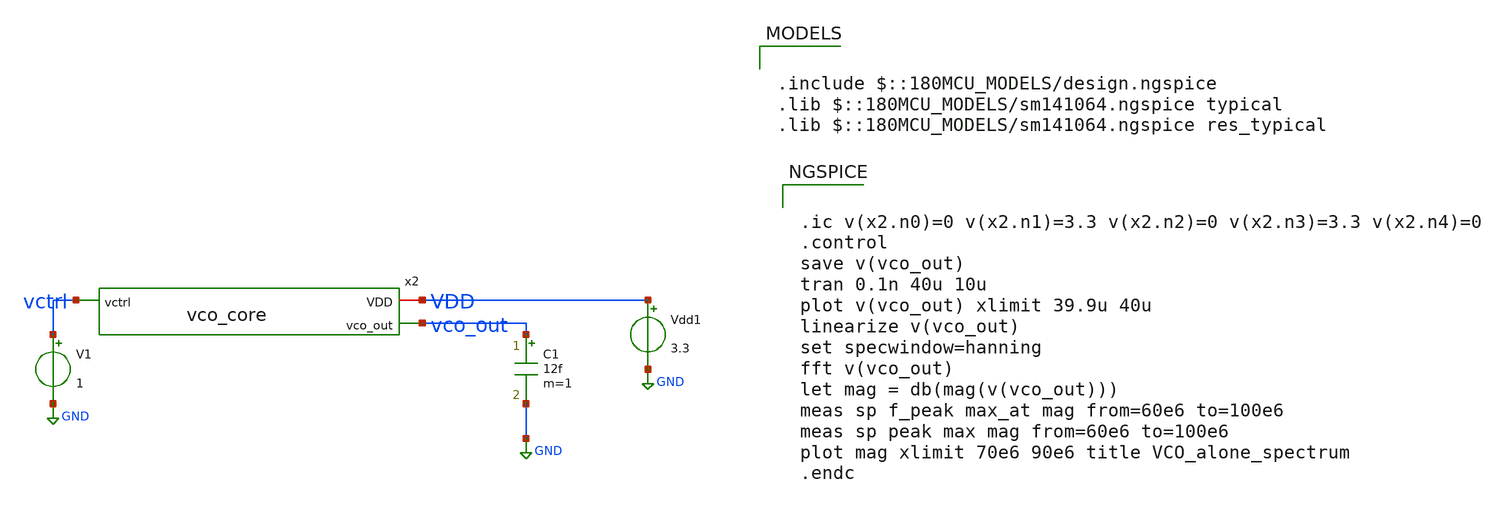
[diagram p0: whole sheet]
** sch_path: xschem/pll_dac/tb_vco_fft.sch
**.subckt tb_vco_fft
x2 VDD vctrl vco_out vco_core
C1 vco_out GND 12f m=1
V1 vctrl GND 1
Vdd1 VDD GND 3.3
**** begin user architecture code

.include $::180MCU_MODELS/design.ngspice
.lib $::180MCU_MODELS/sm141064.ngspice typical
.lib $::180MCU_MODELS/sm141064.ngspice res_typical



.ic v(x2.n0)=0 v(x2.n1)=3.3 v(x2.n2)=0 v(x2.n3)=3.3 v(x2.n4)=0
.control
save v(vco_out)
tran 0.1n 40u 10u
plot v(vco_out) xlimit 39.9u 40u
linearize v(vco_out)
set specwindow=hanning
fft v(vco_out)
let mag = db(mag(v(vco_out)))
meas sp f_peak max_at mag from=60e6 to=100e6
meas sp peak max mag from=60e6 to=100e6
plot mag xlimit 70e6 90e6 title VCO_alone_spectrum
.endc


**** end user architecture code
**.ends

* expanding   symbol:  GF180-PLL/analog/vco/vco_core.sym # of pins=3
** sym_path: analog/vco/vco_core.sym
** sch_path: analog/vco/vco_core.sch
.subckt vco_core VDD vctrl vco_out
*.iopin VDD
*.ipin vctrl
*.opin vco_out
XM1 Vbiasn vctrl net1 net1 pfet_03v3 L=1u W=8u nf=1 ad='int((nf+1)/2) * W/nf * 0.18u' as='int((nf+2)/2) * W/nf * 0.18u'
+ pd='2*int((nf+1)/2) * (W/nf + 0.18u)' ps='2*int((nf+2)/2) * (W/nf + 0.18u)' nrd='0.18u / W' nrs='0.18u / W'
+ sa=0 sb=0 sd=0 m=1
XM2 Vbiasn Vbiasn GND GND nfet_03v3 L=1u W=3u nf=1 ad='int((nf+1)/2) * W/nf * 0.18u' as='int((nf+2)/2) * W/nf * 0.18u'
+ pd='2*int((nf+1)/2) * (W/nf + 0.18u)' ps='2*int((nf+2)/2) * (W/nf + 0.18u)' nrd='0.18u / W' nrs='0.18u / W'
+ sa=0 sb=0 sd=0 m=1
XM3 Vbiasp Vbiasn GND GND nfet_03v3 L=1u W=3u nf=1 ad='int((nf+1)/2) * W/nf * 0.18u' as='int((nf+2)/2) * W/nf * 0.18u'
+ pd='2*int((nf+1)/2) * (W/nf + 0.18u)' ps='2*int((nf+2)/2) * (W/nf + 0.18u)' nrd='0.18u / W' nrs='0.18u / W'
+ sa=0 sb=0 sd=0 m=1
XM4 Vbiasp Vbiasp VDD VDD pfet_03v3 L=1u W=3u nf=1 ad='int((nf+1)/2) * W/nf * 0.18u' as='int((nf+2)/2) * W/nf * 0.18u'
+ pd='2*int((nf+1)/2) * (W/nf + 0.18u)' ps='2*int((nf+2)/2) * (W/nf + 0.18u)' nrd='0.18u / W' nrs='0.18u / W'
+ sa=0 sb=0 sd=0 m=1
XR1 net1 VDD GND ppolyf_u r_width=1u r_length=189u m=1
XM5 net2 Vbiasn GND GND nfet_03v3 L=1u W=3u nf=1 ad='int((nf+1)/2) * W/nf * 0.18u' as='int((nf+2)/2) * W/nf * 0.18u'
+ pd='2*int((nf+1)/2) * (W/nf + 0.18u)' ps='2*int((nf+2)/2) * (W/nf + 0.18u)' nrd='0.18u / W' nrs='0.18u / W'
+ sa=0 sb=0 sd=0 m=1
XM6 n0 n4 net2 GND nfet_03v3 L=0.28u W=1u nf=1 ad='int((nf+1)/2) * W/nf * 0.18u' as='int((nf+2)/2) * W/nf * 0.18u'
+ pd='2*int((nf+1)/2) * (W/nf + 0.18u)' ps='2*int((nf+2)/2) * (W/nf + 0.18u)' nrd='0.18u / W' nrs='0.18u / W'
+ sa=0 sb=0 sd=0 m=1
XM7 n0 n4 net3 VDD pfet_03v3 L=0.28u W=2u nf=1 ad='int((nf+1)/2) * W/nf * 0.18u' as='int((nf+2)/2) * W/nf * 0.18u'
+ pd='2*int((nf+1)/2) * (W/nf + 0.18u)' ps='2*int((nf+2)/2) * (W/nf + 0.18u)' nrd='0.18u / W' nrs='0.18u / W'
+ sa=0 sb=0 sd=0 m=1
XM8 net3 Vbiasp VDD VDD pfet_03v3 L=1u W=3u nf=1 ad='int((nf+1)/2) * W/nf * 0.18u' as='int((nf+2)/2) * W/nf * 0.18u'
+ pd='2*int((nf+1)/2) * (W/nf + 0.18u)' ps='2*int((nf+2)/2) * (W/nf + 0.18u)' nrd='0.18u / W' nrs='0.18u / W'
+ sa=0 sb=0 sd=0 m=1
XM9 net4 Vbiasn GND GND nfet_03v3 L=1u W=3u nf=1 ad='int((nf+1)/2) * W/nf * 0.18u' as='int((nf+2)/2) * W/nf * 0.18u'
+ pd='2*int((nf+1)/2) * (W/nf + 0.18u)' ps='2*int((nf+2)/2) * (W/nf + 0.18u)' nrd='0.18u / W' nrs='0.18u / W'
+ sa=0 sb=0 sd=0 m=1
XM10 n1 n0 net4 GND nfet_03v3 L=0.28u W=1u nf=1 ad='int((nf+1)/2) * W/nf * 0.18u' as='int((nf+2)/2) * W/nf * 0.18u'
+ pd='2*int((nf+1)/2) * (W/nf + 0.18u)' ps='2*int((nf+2)/2) * (W/nf + 0.18u)' nrd='0.18u / W' nrs='0.18u / W'
+ sa=0 sb=0 sd=0 m=1
XM11 n1 n0 net5 VDD pfet_03v3 L=0.28u W=2u nf=1 ad='int((nf+1)/2) * W/nf * 0.18u' as='int((nf+2)/2) * W/nf * 0.18u'
+ pd='2*int((nf+1)/2) * (W/nf + 0.18u)' ps='2*int((nf+2)/2) * (W/nf + 0.18u)' nrd='0.18u / W' nrs='0.18u / W'
+ sa=0 sb=0 sd=0 m=1
XM12 net5 Vbiasp VDD VDD pfet_03v3 L=1u W=3u nf=1 ad='int((nf+1)/2) * W/nf * 0.18u' as='int((nf+2)/2) * W/nf * 0.18u'
+ pd='2*int((nf+1)/2) * (W/nf + 0.18u)' ps='2*int((nf+2)/2) * (W/nf + 0.18u)' nrd='0.18u / W' nrs='0.18u / W'
+ sa=0 sb=0 sd=0 m=1
XM13 net6 Vbiasn GND GND nfet_03v3 L=1u W=3u nf=1 ad='int((nf+1)/2) * W/nf * 0.18u' as='int((nf+2)/2) * W/nf * 0.18u'
+ pd='2*int((nf+1)/2) * (W/nf + 0.18u)' ps='2*int((nf+2)/2) * (W/nf + 0.18u)' nrd='0.18u / W' nrs='0.18u / W'
+ sa=0 sb=0 sd=0 m=1
XM14 n2 n1 net6 GND nfet_03v3 L=0.28u W=1u nf=1 ad='int((nf+1)/2) * W/nf * 0.18u' as='int((nf+2)/2) * W/nf * 0.18u'
+ pd='2*int((nf+1)/2) * (W/nf + 0.18u)' ps='2*int((nf+2)/2) * (W/nf + 0.18u)' nrd='0.18u / W' nrs='0.18u / W'
+ sa=0 sb=0 sd=0 m=1
XM15 n2 n1 net7 VDD pfet_03v3 L=0.28u W=2u nf=1 ad='int((nf+1)/2) * W/nf * 0.18u' as='int((nf+2)/2) * W/nf * 0.18u'
+ pd='2*int((nf+1)/2) * (W/nf + 0.18u)' ps='2*int((nf+2)/2) * (W/nf + 0.18u)' nrd='0.18u / W' nrs='0.18u / W'
+ sa=0 sb=0 sd=0 m=1
XM16 net7 Vbiasp VDD VDD pfet_03v3 L=1u W=3u nf=1 ad='int((nf+1)/2) * W/nf * 0.18u' as='int((nf+2)/2) * W/nf * 0.18u'
+ pd='2*int((nf+1)/2) * (W/nf + 0.18u)' ps='2*int((nf+2)/2) * (W/nf + 0.18u)' nrd='0.18u / W' nrs='0.18u / W'
+ sa=0 sb=0 sd=0 m=1
XM17 net8 Vbiasn GND GND nfet_03v3 L=1u W=3u nf=1 ad='int((nf+1)/2) * W/nf * 0.18u' as='int((nf+2)/2) * W/nf * 0.18u'
+ pd='2*int((nf+1)/2) * (W/nf + 0.18u)' ps='2*int((nf+2)/2) * (W/nf + 0.18u)' nrd='0.18u / W' nrs='0.18u / W'
+ sa=0 sb=0 sd=0 m=1
XM18 n3 n2 net8 GND nfet_03v3 L=0.28u W=1u nf=1 ad='int((nf+1)/2) * W/nf * 0.18u' as='int((nf+2)/2) * W/nf * 0.18u'
+ pd='2*int((nf+1)/2) * (W/nf + 0.18u)' ps='2*int((nf+2)/2) * (W/nf + 0.18u)' nrd='0.18u / W' nrs='0.18u / W'
+ sa=0 sb=0 sd=0 m=1
XM19 n3 n2 net9 VDD pfet_03v3 L=0.28u W=2u nf=1 ad='int((nf+1)/2) * W/nf * 0.18u' as='int((nf+2)/2) * W/nf * 0.18u'
+ pd='2*int((nf+1)/2) * (W/nf + 0.18u)' ps='2*int((nf+2)/2) * (W/nf + 0.18u)' nrd='0.18u / W' nrs='0.18u / W'
+ sa=0 sb=0 sd=0 m=1
XM20 net9 Vbiasp VDD VDD pfet_03v3 L=1u W=3u nf=1 ad='int((nf+1)/2) * W/nf * 0.18u' as='int((nf+2)/2) * W/nf * 0.18u'
+ pd='2*int((nf+1)/2) * (W/nf + 0.18u)' ps='2*int((nf+2)/2) * (W/nf + 0.18u)' nrd='0.18u / W' nrs='0.18u / W'
+ sa=0 sb=0 sd=0 m=1
XM21 net10 Vbiasn GND GND nfet_03v3 L=1u W=3u nf=1 ad='int((nf+1)/2) * W/nf * 0.18u' as='int((nf+2)/2) * W/nf * 0.18u'
+ pd='2*int((nf+1)/2) * (W/nf + 0.18u)' ps='2*int((nf+2)/2) * (W/nf + 0.18u)' nrd='0.18u / W' nrs='0.18u / W'
+ sa=0 sb=0 sd=0 m=1
XM22 n4 n3 net10 GND nfet_03v3 L=0.28u W=1u nf=1 ad='int((nf+1)/2) * W/nf * 0.18u' as='int((nf+2)/2) * W/nf * 0.18u'
+ pd='2*int((nf+1)/2) * (W/nf + 0.18u)' ps='2*int((nf+2)/2) * (W/nf + 0.18u)' nrd='0.18u / W' nrs='0.18u / W'
+ sa=0 sb=0 sd=0 m=1
XM23 n4 n3 net11 VDD pfet_03v3 L=0.28u W=2u nf=1 ad='int((nf+1)/2) * W/nf * 0.18u' as='int((nf+2)/2) * W/nf * 0.18u'
+ pd='2*int((nf+1)/2) * (W/nf + 0.18u)' ps='2*int((nf+2)/2) * (W/nf + 0.18u)' nrd='0.18u / W' nrs='0.18u / W'
+ sa=0 sb=0 sd=0 m=1
XM24 net11 Vbiasp VDD VDD pfet_03v3 L=1u W=3u nf=1 ad='int((nf+1)/2) * W/nf * 0.18u' as='int((nf+2)/2) * W/nf * 0.18u'
+ pd='2*int((nf+1)/2) * (W/nf + 0.18u)' ps='2*int((nf+2)/2) * (W/nf + 0.18u)' nrd='0.18u / W' nrs='0.18u / W'
+ sa=0 sb=0 sd=0 m=1
C1 n0 GND 3f m=1
C2 n1 GND 3f m=1
C3 n2 GND 3f m=1
C4 n3 GND 3f m=1
C5 n4 GND 3f m=1
XM25 net12 n4 GND GND nfet_03v3 L=0.28u W=1u nf=1 ad='int((nf+1)/2) * W/nf * 0.18u' as='int((nf+2)/2) * W/nf * 0.18u'
+ pd='2*int((nf+1)/2) * (W/nf + 0.18u)' ps='2*int((nf+2)/2) * (W/nf + 0.18u)' nrd='0.18u / W' nrs='0.18u / W'
+ sa=0 sb=0 sd=0 m=1
XM26 net12 n4 VDD VDD pfet_03v3 L=0.28u W=2u nf=1 ad='int((nf+1)/2) * W/nf * 0.18u' as='int((nf+2)/2) * W/nf * 0.18u'
+ pd='2*int((nf+1)/2) * (W/nf + 0.18u)' ps='2*int((nf+2)/2) * (W/nf + 0.18u)' nrd='0.18u / W' nrs='0.18u / W'
+ sa=0 sb=0 sd=0 m=1
XM27 vco_out net12 GND GND nfet_03v3 L=0.28u W=1u nf=1 ad='int((nf+1)/2) * W/nf * 0.18u' as='int((nf+2)/2) * W/nf * 0.18u'
+ pd='2*int((nf+1)/2) * (W/nf + 0.18u)' ps='2*int((nf+2)/2) * (W/nf + 0.18u)' nrd='0.18u / W' nrs='0.18u / W'
+ sa=0 sb=0 sd=0 m=1
XM28 vco_out net12 VDD VDD pfet_03v3 L=0.28u W=2u nf=1 ad='int((nf+1)/2) * W/nf * 0.18u' as='int((nf+2)/2) * W/nf * 0.18u'
+ pd='2*int((nf+1)/2) * (W/nf + 0.18u)' ps='2*int((nf+2)/2) * (W/nf + 0.18u)' nrd='0.18u / W' nrs='0.18u / W'
+ sa=0 sb=0 sd=0 m=1
C7 net12 GND 3f m=1
.ends

.GLOBAL GND
.end
